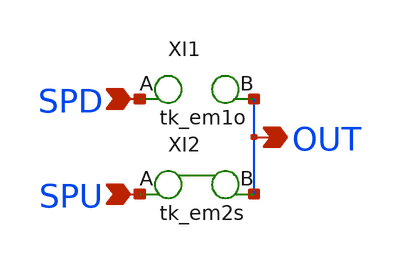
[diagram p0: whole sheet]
** sch_path: common/tk_optiA.sch
* Copyright 2023 David Mitchell Bailey
* Licensed under the Apache License, Version 2.0 (the "License");
* you may not use this file except in compliance with the License.
* You may obtain a copy of the License at
* https://www.apache.org/licenses/LICENSE-2.0
* Unless required by applicable law or agreed to in writing, software
* distributed under the License is distributed on an "AS IS" BASIS,
* WITHOUT WARRANTIES OR CONDITIONS OF ANY KIND, either express or implied.
* See the License for the specific language governing permissions and
* limitations under the License.
**.subckt tk_optiA SPU SPD OUT
*.ipin SPU
*.ipin SPD
*.opin OUT
XI1 SPD OUT tk_em1o
XI2 SPU OUT tk_em2s
**.ends

* expanding   symbol:  common/tk_em1o.sym # of pins=2
** sym_path: common/tk_em1o.sym
** sch_path: common/tk_em1o.sch
.subckt tk_em1o A B
*.iopin A
*.iopin B
R1 net1 A sky130_fd_pr__res_generic_m1 W=0.66 L=0.01 m=1
R2 B net2 sky130_fd_pr__res_generic_m1 W=0.66 L=0.01 m=1
* noconn #net1
* noconn #net2
.ends


* expanding   symbol:  common/tk_em2s.sym # of pins=2
** sym_path: common/tk_em2s.sym
** sch_path: common/tk_em2s.sch
.subckt tk_em2s A B
*.iopin A
*.iopin B
R1 net1 A sky130_fd_pr__res_generic_m2 W=0.26 L=0.01 m=1
R2 B net1 sky130_fd_pr__res_generic_m2 W=0.26 L=0.01 m=1
.ends

.end
